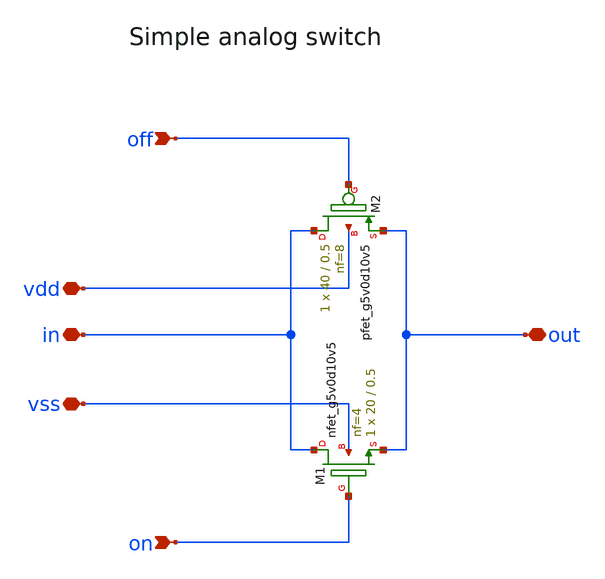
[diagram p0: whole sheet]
** sch_path: analog/repairs/adc_repaired/base/ip/sky130_ef_ip__cdac3v_12bit/dependencies/sky130_ef_ip__analog_switches/xschem/simple_analog_switch_2.sch
**.subckt simple_analog_switch_2 on out vdd vss in off
*.ipin on
*.iopin out
*.iopin vdd
*.iopin vss
*.iopin in
*.ipin off
XM1 in on out vss sky130_fd_pr__nfet_g5v0d10v5 L=0.5 W=20 nf=4 ad='int((nf+1)/2) * W/nf * 0.29' as='int((nf+2)/2) * W/nf * 0.29'
+ pd='2*int((nf+1)/2) * (W/nf + 0.29)' ps='2*int((nf+2)/2) * (W/nf + 0.29)' nrd='0.29 / W' nrs='0.29 / W'
+ sa=0 sb=0 sd=0 mult=1 m=1
XM2 in off out vdd sky130_fd_pr__pfet_g5v0d10v5 L=0.5 W=40 nf=8 ad='int((nf+1)/2) * W/nf * 0.29' as='int((nf+2)/2) * W/nf * 0.29'
+ pd='2*int((nf+1)/2) * (W/nf + 0.29)' ps='2*int((nf+2)/2) * (W/nf + 0.29)' nrd='0.29 / W' nrs='0.29 / W'
+ sa=0 sb=0 sd=0 mult=1 m=1
**.ends
.end
